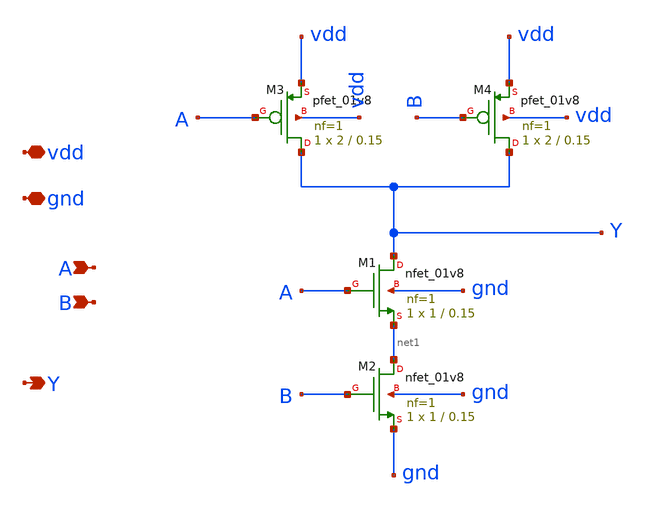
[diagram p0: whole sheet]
** sch_path: LogicGates/nand.sch
**.subckt nand A B vdd gnd Y
*.ipin A
*.ipin B
*.iopin vdd
*.iopin gnd
*.opin Y
XM1 Y A net1 gnd sky130_fd_pr__nfet_01v8 L=0.15 W=1 nf=1 ad='int((nf+1)/2) * W/nf * 0.29' as='int((nf+2)/2) * W/nf * 0.29'
+ pd='2*int((nf+1)/2) * (W/nf + 0.29)' ps='2*int((nf+2)/2) * (W/nf + 0.29)' nrd='0.29 / W' nrs='0.29 / W'
+ sa=0 sb=0 sd=0 mult=1 m=1
XM2 net1 B gnd gnd sky130_fd_pr__nfet_01v8 L=0.15 W=1 nf=1 ad='int((nf+1)/2) * W/nf * 0.29' as='int((nf+2)/2) * W/nf * 0.29'
+ pd='2*int((nf+1)/2) * (W/nf + 0.29)' ps='2*int((nf+2)/2) * (W/nf + 0.29)' nrd='0.29 / W' nrs='0.29 / W'
+ sa=0 sb=0 sd=0 mult=1 m=1
XM3 Y A vdd vdd sky130_fd_pr__pfet_01v8 L=0.15 W=2 nf=1 ad='int((nf+1)/2) * W/nf * 0.29' as='int((nf+2)/2) * W/nf * 0.29'
+ pd='2*int((nf+1)/2) * (W/nf + 0.29)' ps='2*int((nf+2)/2) * (W/nf + 0.29)' nrd='0.29 / W' nrs='0.29 / W'
+ sa=0 sb=0 sd=0 mult=1 m=1
XM4 Y B vdd vdd sky130_fd_pr__pfet_01v8 L=0.15 W=2 nf=1 ad='int((nf+1)/2) * W/nf * 0.29' as='int((nf+2)/2) * W/nf * 0.29'
+ pd='2*int((nf+1)/2) * (W/nf + 0.29)' ps='2*int((nf+2)/2) * (W/nf + 0.29)' nrd='0.29 / W' nrs='0.29 / W'
+ sa=0 sb=0 sd=0 mult=1 m=1
**.ends
.end
